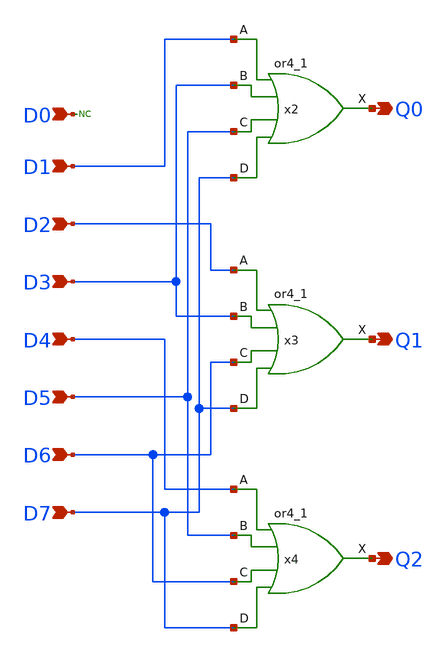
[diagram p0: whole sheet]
** sch_path: PriorityEncoder/3to8_Priority_Encoder_v0p1p1.sch
.lib $::SKYWATER_MODELS/sky130.lib.spice tt
.include $::SKYWATER_STDCELLS/sky130_fd_sc_hd.spice

**.subckt 3to8_Priority_Encoder_v0p1p1 D2 D3 D4 D5 D6 D7 D1 D0 Q0 Q1 Q2
*.ipin D2
*.ipin D3
*.ipin D4
*.ipin D5
*.ipin D6
*.ipin D7
*.ipin D1
*.ipin D0
*.opin Q0
*.opin Q1
*.opin Q2
* noconn D0
x2 D1 D3 D5 D7 GND GND VDD VDD Q0 sky130_fd_sc_hd__or4_1
x3 D2 D3 D6 D7 GND GND VDD VDD Q1 sky130_fd_sc_hd__or4_1
x4 D4 D5 D6 D7 GND GND VDD VDD Q2 sky130_fd_sc_hd__or4_1
**.ends
.end
